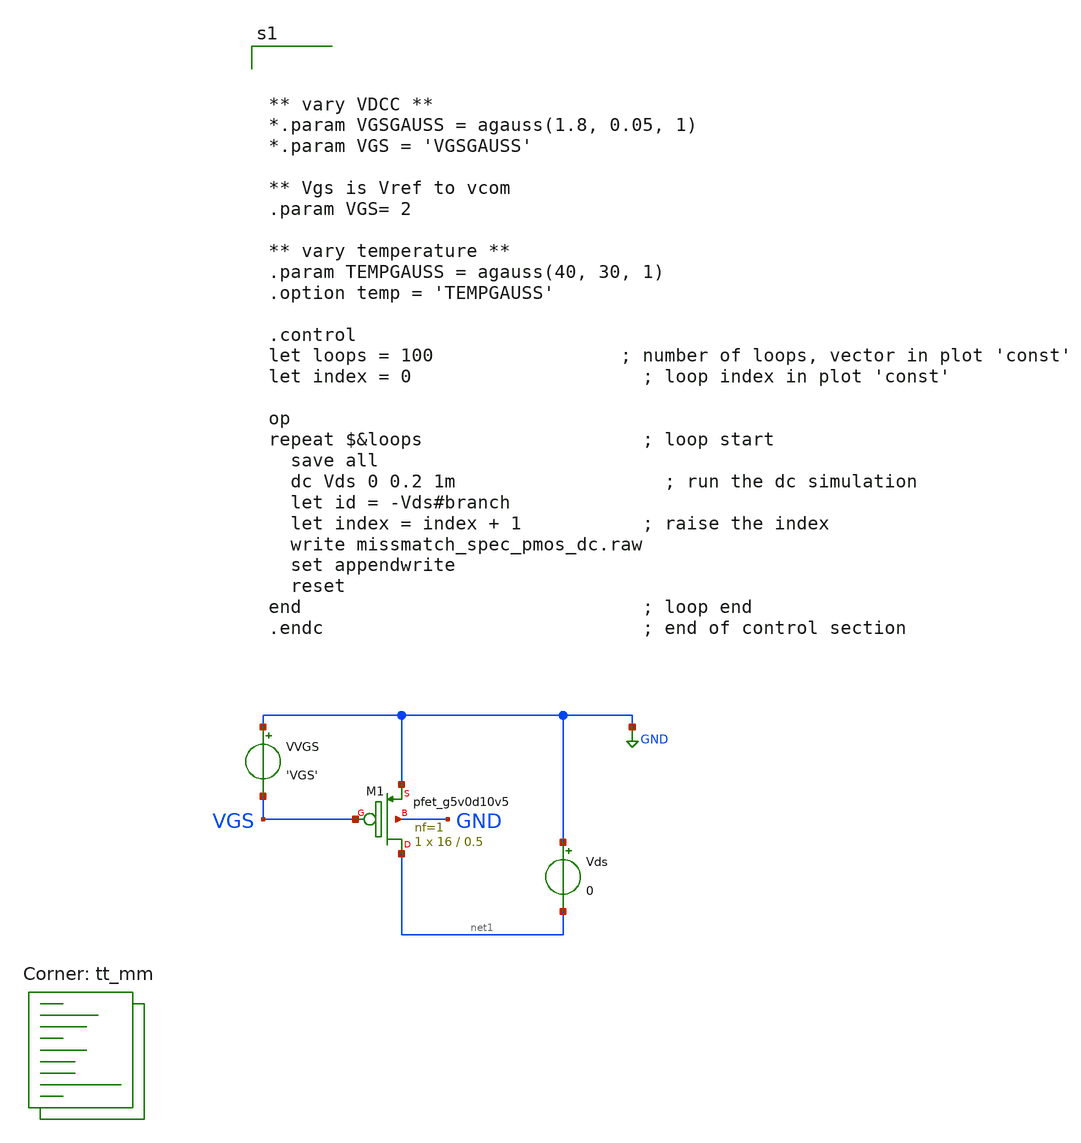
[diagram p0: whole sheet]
** sch_path: xschem/missmatch_spec_pmos_dc.sch
**.subckt missmatch_spec_pmos_dc
VVGS GND VGS 'VGS'
Vds GND net1 0
XM1 net1 VGS GND GND sky130_fd_pr__pfet_g5v0d10v5 L=0.5 W=16 nf=1 ad='int((nf+1)/2) * W/nf * 0.29' as='int((nf+2)/2) * W/nf * 0.29'
+ pd='2*int((nf+1)/2) * (W/nf + 0.29)' ps='2*int((nf+2)/2) * (W/nf + 0.29)' nrd='0.29 / W' nrs='0.29 / W'
+ sa=0 sb=0 sd=0 mult=1 m=1
**** begin user architecture code
.lib $::SKYWATER_MODELS/sky130.lib.spice tt_mm



** vary VDCC **
*.param VGSGAUSS = agauss(1.8, 0.05, 1)
*.param VGS = 'VGSGAUSS'

** Vgs is Vref to vcom
.param VGS= 2

** vary temperature **
.param TEMPGAUSS = agauss(40, 30, 1)
.option temp = 'TEMPGAUSS'

.control
let loops = 100                 ; number of loops, vector in plot 'const'
let index = 0                     ; loop index in plot 'const'

op
repeat $&loops                    ; loop start
  save all
  dc Vds 0 0.2 1m                   ; run the dc simulation
  let id = -Vds#branch
  let index = index + 1           ; raise the index
  write missmatch_spec_pmos_dc.raw
  set appendwrite
  reset
end                               ; loop end
.endc                             ; end of control section


**** end user architecture code
**.ends
.GLOBAL GND
.end
